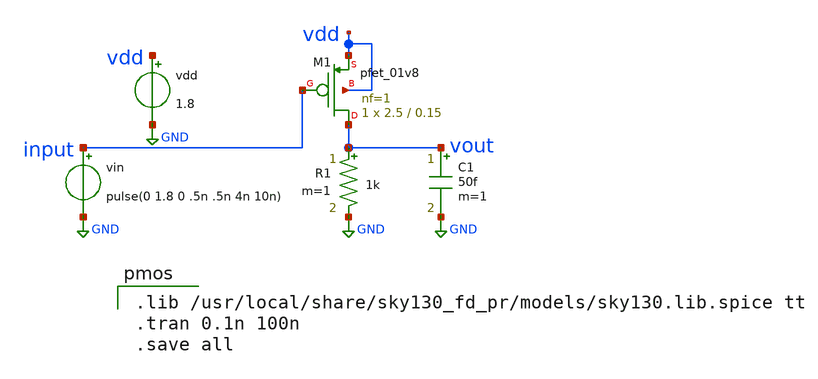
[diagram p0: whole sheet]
** sch_path: files/mos_characteristics/week0_strong1/pmos.sch
**.subckt pmos
XM1 vout input vdd vdd sky130_fd_pr__pfet_01v8 L=0.15 W=2.5 nf=1 ad='int((1 + 1)/2) * 2.5 / 1 * 0.29'
+ as='int((1 + 2)/2) * 2.5 / 1 * 0.29' pd='2*int((1 + 1)/2) * (2.5 / 1 + 0.29)' ps='2*int((1 + 2)/2) * (2.5 / 1 + 0.29)'
+ nrd='0.29 / 2.5 ' nrs='0.29 / 2.5 ' sa=0 sb=0 sd=0 mult=1 m=1
R1 vout GND 1k m=1
C1 vout GND 50f m=1
vin input GND pulse(0 1.8 0 .5n .5n 4n 10n)
vdd vdd GND 1.8
**** begin user architecture code

.lib /usr/local/share/sky130_fd_pr/models/sky130.lib.spice tt
.tran 0.1n 100n
.save all

**** end user architecture code
**.ends
.GLOBAL GND
.end
